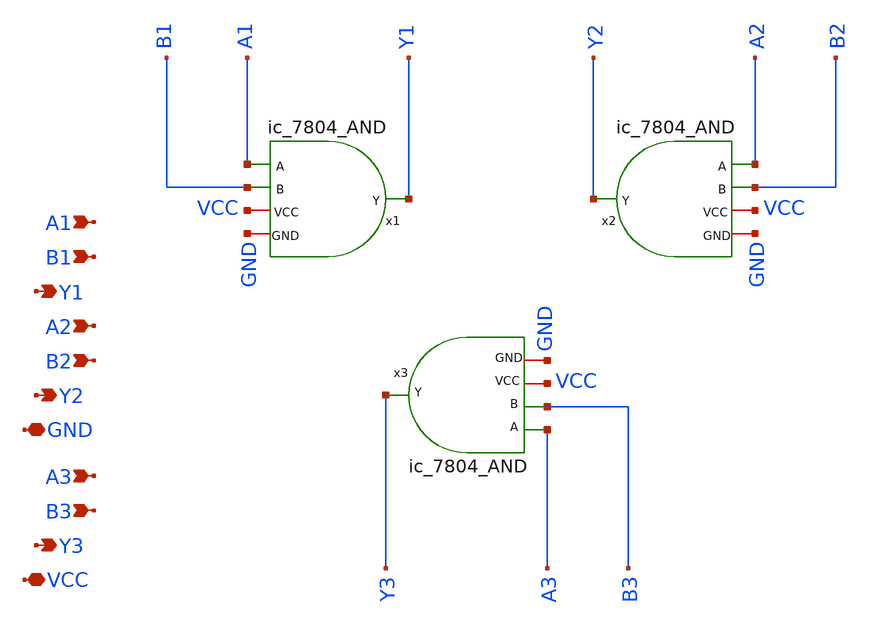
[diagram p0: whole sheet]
** sch_path: xschem/AND_IC_TopLevel.sch
**.subckt AND_IC_TopLevel A1 GND Y1 B1 A2 B2 A3 Y2 Y3 VCC B3
*.ipin A1
*.iopin GND
*.opin Y1
*.ipin B1
*.ipin A2
*.ipin B2
*.ipin A3
*.opin Y2
*.opin Y3
*.iopin VCC
*.ipin B3
x1 A1 B1 Y1 VCC GND ic_7804_AND
x2 A2 B2 Y2 VCC GND ic_7804_AND
x3 A3 B3 Y3 VCC GND ic_7804_AND
**.ends

* expanding   symbol:  ic_7804_AND.sym # of pins=5
** sym_path: xschem/ic_7804_AND.sym
** sch_path: xschem/ic_7804_AND.sch
.subckt ic_7804_AND A B Y VCC GND
*.ipin A
*.opin Y
*.ipin B
*.iopin VCC
*.iopin GND
XM2 net1 A VCC VCC sky130_fd_pr__pfet_01v8 L=0.15 W=2 nf=1 ad='int((nf+1)/2) * W/nf * 0.29' as='int((nf+2)/2) * W/nf * 0.29'
+ pd='2*int((nf+1)/2) * (W/nf + 0.29)' ps='2*int((nf+2)/2) * (W/nf + 0.29)' nrd='0.29 / W' nrs='0.29 / W'
+ sa=0 sb=0 sd=0 mult=1 m=1
XM3 net1 B VCC VCC sky130_fd_pr__pfet_01v8 L=0.15 W=2 nf=1 ad='int((nf+1)/2) * W/nf * 0.29' as='int((nf+2)/2) * W/nf * 0.29'
+ pd='2*int((nf+1)/2) * (W/nf + 0.29)' ps='2*int((nf+2)/2) * (W/nf + 0.29)' nrd='0.29 / W' nrs='0.29 / W'
+ sa=0 sb=0 sd=0 mult=1 m=1
XM5 Y net1 VCC VCC sky130_fd_pr__pfet_01v8 L=0.15 W=2 nf=1 ad='int((nf+1)/2) * W/nf * 0.29' as='int((nf+2)/2) * W/nf * 0.29'
+ pd='2*int((nf+1)/2) * (W/nf + 0.29)' ps='2*int((nf+2)/2) * (W/nf + 0.29)' nrd='0.29 / W' nrs='0.29 / W'
+ sa=0 sb=0 sd=0 mult=1 m=1
XM1 net1 A net2 GND sky130_fd_pr__nfet_01v8 L=0.15 W=1 nf=1 ad='int((nf+1)/2) * W/nf * 0.29' as='int((nf+2)/2) * W/nf * 0.29'
+ pd='2*int((nf+1)/2) * (W/nf + 0.29)' ps='2*int((nf+2)/2) * (W/nf + 0.29)' nrd='0.29 / W' nrs='0.29 / W'
+ sa=0 sb=0 sd=0 mult=1 m=1
XM4 net2 B GND GND sky130_fd_pr__nfet_01v8 L=0.15 W=1 nf=1 ad='int((nf+1)/2) * W/nf * 0.29' as='int((nf+2)/2) * W/nf * 0.29'
+ pd='2*int((nf+1)/2) * (W/nf + 0.29)' ps='2*int((nf+2)/2) * (W/nf + 0.29)' nrd='0.29 / W' nrs='0.29 / W'
+ sa=0 sb=0 sd=0 mult=1 m=1
XM6 Y net1 GND GND sky130_fd_pr__nfet_01v8 L=0.15 W=1 nf=1 ad='int((nf+1)/2) * W/nf * 0.29' as='int((nf+2)/2) * W/nf * 0.29'
+ pd='2*int((nf+1)/2) * (W/nf + 0.29)' ps='2*int((nf+2)/2) * (W/nf + 0.29)' nrd='0.29 / W' nrs='0.29 / W'
+ sa=0 sb=0 sd=0 mult=1 m=1
.ends

.end
